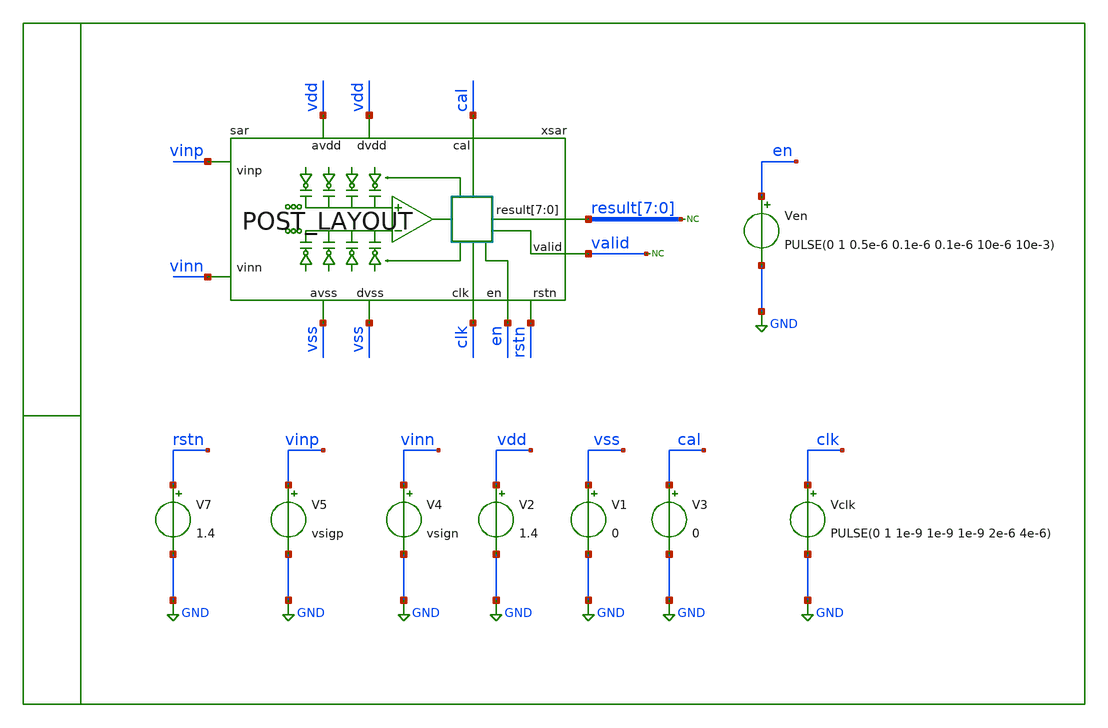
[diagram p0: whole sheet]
** sch_path: xschem/tb/sar/tr_sar.sch
**.subckt tr_sar
V1 vss GND 0
V2 vdd GND 1.4
V4 vinn GND vsign
V5 vinp GND vsigp
Vclk clk GND PULSE(0 1 1e-9 1e-9 1e-9 2e-6 4e-6)
Ven en GND PULSE(0 1 0.5e-6 0.1e-6 0.1e-6 10e-6 10e-3)
* noconn valid
V3 cal GND 0
* noconn result[7:0]
xsar vdd vdd vss result[7] result[6] result[5] result[4] result[3] result[2] result[1] result[0]
+ vinn vss clk vinp en valid cal rstn sar
V7 rstn GND 1.4
**** begin user architecture code

.include $::SKYWATER_STDCELLS/sky130_fd_sc_hd.spice
*.include $::SKYWATER_STDCELLS/cells/inv/sky130_fd_sc_hd__inv_4.spice
*.include $::SKYWATER_STDCELLS/cells/decap/sky130_fd_sc_hd__decap_8.spice
*.include $::SKYWATER_STDCELLS/cells/decap/sky130_fd_sc_hd__decap_3.spice
*.include $::SKYWATER_STDCELLS/cells/buf/sky130_fd_sc_hd__buf_1.spice
*.include $::SKYWATER_STDCELLS/cells/inv/sky130_fd_sc_hd__inv_1.spice
*.include $::SKYWATER_STDCELLS/cells/inv/sky130_fd_sc_hd__inv_2.spice
*.include $::SKYWATER_STDCELLS/cells/tap/sky130_fd_sc_hd__tap_2.spice

 .options method trap
*.options method gear
.options gmin 1e-15
.options abstol 1e-15
.options reltol 0.0001
.options vntol 0.1e-6
.options warn 1

.param MC_SWITCH=0
.param vin=1
.param vcm=0.7
.param vsigp=1.2
.param vsign=0.2

.tran 100e-9 48e-6

.control

run

meas tran d0 find v(xsar.res0) at=47e-6
meas tran d1 find v(xsar.res1) at=47e-6
meas tran d2 find v(xsar.res2) at=47e-6
meas tran d3 find v(xsar.res3) at=47e-6
meas tran d4 find v(xsar.res4) at=47e-6
meas tran d5 find v(xsar.res5) at=47e-6
meas tran d6 find v(xsar.res6) at=47e-6
meas tran d7 find v(xsar.res7) at=47e-6

* meas tran d0 find v(xsar.result0) at=47e-6
* meas tran d1 find v(xsar.result1) at=47e-6
* meas tran d2 find v(xsar.result2) at=47e-6
* meas tran d3 find v(xsar.result3) at=47e-6
* meas tran d4 find v(xsar.result4) at=47e-6
* meas tran d5 find v(xsar.result5) at=47e-6
* meas tran d6 find v(xsar.result6) at=47e-6
* meas tran d7 find v(xsar.result7) at=47e-6

meas tran vpmax max xsar.vp
meas tran vpmin min xsar.vp
meas tran vpend find v(xsar.vp) at=39e-6

meas tran vnmax max xsar.vn
meas tran vnmin min xsar.vn
meas tran vnend find v(xsar.vn) at=39e-6

print d0
print d1
print d2
print d3
print d4
print d5
print d6
print d7

print vpmax
print vpmin

print vnmax
print vnmin

print vpend
print vnend

.endc
 * FET CORNERS
*.include $::SKYWATER_MODELS/corners/tt.spice
*.include $::SKYWATER_MODELS/corners/ff.spice
*.include $::SKYWATER_MODELS/corners/ss.spice
*.include $::SKYWATER_MODELS/corners/sf.spice
*.include $::SKYWATER_MODELS/corners/fs.spice

* TT + R + C
*.include $::SKYWATER_MODELS/corners/tt_rmax_cmax.spice
*.include $::SKYWATER_MODELS/corners/tt_rmin_cmin.spice
*.include $::SKYWATER_MODELS/corners/tt_rmax_cmin.spice
*.include $::SKYWATER_MODELS/corners/tt_rmin_cmax.spice

* FF + R + C
*.include $::SKYWATER_MODELS/corners/ff_rmax_cmax.spice
*.include $::SKYWATER_MODELS/corners/ff_rmin_cmin.spice
*.include $::SKYWATER_MODELS/corners/ff_rmax_cmin.spice
*.include $::SKYWATER_MODELS/corners/ff_rmin_cmax.spice


* SS + R + C
*.include $::SKYWATER_MODELS/corners/ss_rmax_cmax.spice
*.include $::SKYWATER_MODELS/corners/ss_rmin_cmin.spice
*.include $::SKYWATER_MODELS/corners/ss_rmax_cmin.spice
*.include $::SKYWATER_MODELS/corners/ss_rmin_cmax.spice

* SF + R + C
*.include $::SKYWATER_MODELS/corners/sf_rmax_cmax.spice
*.include $::SKYWATER_MODELS/corners/sf_rmin_cmin.spice
*.include $::SKYWATER_MODELS/corners/sf_rmax_cmin.spice
*.include $::SKYWATER_MODELS/corners/sf_rmin_cmax.spice

* FS + R + C
*.include $::SKYWATER_MODELS/corners/fs_rmax_cmax.spice
*.include $::SKYWATER_MODELS/corners/fs_rmin_cmin.spice
*.include $::SKYWATER_MODELS/corners/fs_rmax_cmin.spice
*.include $::SKYWATER_MODELS/corners/fs_rmin_cmax.spice

** opencircuitdesign pdks install
.lib $::SKYWATER_MODELS/sky130.lib.spice tt


**** end user architecture code
**.ends

* expanding   symbol:  sar/sar/sar.sym # of pins=12
** sym_path: xschem/sar/SAR_POSTLAYOUT/sar.sym
** sch_path: xschem/sar/SAR_POSTLAYOUT/sar.sch
.subckt sar avdd dvdd dvss result[7] result[6] result[5] result[4] result[3] result[2] result[1]
+ result[0] vinn avss clk vinp en valid cal rstn
*.iopin avss
*.iopin avdd
*.iopin dvss
*.iopin dvdd
*.ipin vinp
*.ipin vinn
*.opin result[7],result[6],result[5],result[4],result[3],result[2],result[1],result[0]
*.ipin clk
*.ipin en
*.opin valid
*.ipin cal
*.ipin rstn
* noconn comp
**** begin user architecture code

*.include $::DESIGN_PATH/sar/control/cmos_cells_digital.sp
*.include $::DESIGN_PATH/sar/control/sar_logic.sp
*.include $::DESIGN_PATH/sar/control/sar_logic_sky.sp
.include $::DESIGN_PATH/sar/SAR_POSTLAYOUT/user_analog_project_wrapper.spice

**** end user architecture code
* noconn sample
* noconn ctln[7:0]
* noconn ctlp[7:0]
* noconn trim[4:0]
* noconn trimb[4:0]
* noconn result[7:0]
* noconn valid
* noconn clkc
* noconn clk
* noconn en
* noconn cal
* noconn rstn
**** begin user architecture code


**Xuut dclk drstn den dcomp dcal dvalid dres0 dres1 dres2 dres3 dres4 dres5 dres6 dres7 dsamp dctlp0
*+ dctlp1 dctlp2 dctlp3 dctlp4 dctlp5 dctlp6 dctlp7 dctln0 dctln1 dctln2 dctln3 dctln4 dctln5 dctln6 dctln7
*+ dtrim0 dtrim1 dtrim2 dtrim3 dtrim4 dtrimb0 dtrimb1 dtrimb2 dtrimb3 dtrimb4 dclkc sar_logic

.model adc_buff adc_bridge(in_low = 0.2 in_high=0.8)
.model dac_buff dac_bridge(out_high = 1.2)

Aad [clk rstn en comp cal] [dclk drstn den dcomp dcal] adc_buff
Ada [dctlp0 dctlp1 dctlp2 dctlp3 dctlp4 dctlp5 dctlp6 dctlp7 dctln0 dctln1 dctln2 dctln3 dctln4
+ dctln5 dctln6 dctln7 dres0 dres1 dres2 dres3 dres4 dres5 dres6 dres7 dsamp dclkc] [ctlp_0_ ctlp_1_ ctlp_2_
+ ctlp_3_ ctlp_4_ ctlp_5_ ctlp_6_ ctlp_7_ ctln_0_ ctln_1_ ctln_2_ ctln_3_ ctln_4_ ctln_5_ ctln_6_ ctln_7_
+ res0 res1 res2 res3 res4 res5 res6 res7 sample clkc] dac_buff
Ada2 [dtrim4 dtrim3 dtrim2 dtrim1 dtrim0 dtrimb4 dtrimb3 dtrimb2 dtrimb1 dtrimb0] [trim_4_ trim_3_
+ trim_2_ trim_1_ trim_0_ trimb_4_ trimb_3_ trimb_2_ trimb_1_ trimb_0_ ] dac_buff


xsar dcomp dctln1 dctln0 dctlp1 dctlp0 dctln7 dctln6 dctln5 dctln4 dctln3 dctln2 dtrim4  dtrim1
+ dtrim0 dtrim2 dtrim3 dtrimb3 dtrimb2 dtrimb0 dtrimb1 dtrimb4 dctlp2 dctlp3 dctlp4 dctlp5  dctlp6 dctlp7
+ dclkc dres7 dres6 dres5 dres4 drstn dres3 dres2 dres1 dres0  dvalid dcal den dclk vinp vinn dvdd avdd
+ dvss SAR


**** end user architecture code
.ends

.GLOBAL GND
.end
